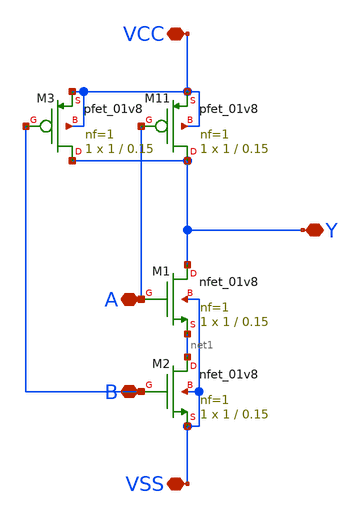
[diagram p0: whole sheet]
** sch_path: logic gates/nand.sch
**.subckt nand VCC VSS Y A B
*.iopin VCC
*.iopin VSS
*.iopin Y
*.iopin A
*.iopin B
XM2 net1 B VSS VSS sky130_fd_pr__nfet_01v8 L=0.15 W=1 nf=1 ad='int((1 + 1)/2) * 1 / 1 * 0.29' as='int((1 + 2)/2) * 1 / 1 * 0.29'
+ pd='2*int((1 + 1)/2) * (1 / 1 + 0.29)' ps='2*int((1 + 2)/2) * (1 / 1 + 0.29)' nrd='0.29 / 1 ' nrs='0.29 / 1 '
+ sa=0 sb=0 sd=0 mult=1 m=1
XM11 Y A VCC VCC sky130_fd_pr__pfet_01v8 L=0.15 W=1 nf=1 ad='int((nf+1)/2) * W/nf * 0.29' as='int((nf+2)/2) * W/nf * 0.29'
+ pd='2*int((nf+1)/2) * (W/nf + 0.29)' ps='2*int((nf+2)/2) * (W/nf + 0.29)' nrd='0.29 / W' nrs='0.29 / W'
+ sa=0 sb=0 sd=0 mult=1 m=1
XM1 Y A net1 VSS sky130_fd_pr__nfet_01v8 L=0.15 W=1 nf=1 ad='int((1 + 1)/2) * 1 / 1 * 0.29' as='int((1 + 2)/2) * 1 / 1 * 0.29'
+ pd='2*int((1 + 1)/2) * (1 / 1 + 0.29)' ps='2*int((1 + 2)/2) * (1 / 1 + 0.29)' nrd='0.29 / 1 ' nrs='0.29 / 1 '
+ sa=0 sb=0 sd=0 mult=1 m=1
XM3 Y B VCC VCC sky130_fd_pr__pfet_01v8 L=0.15 W=1 nf=1 ad='int((nf+1)/2) * W/nf * 0.29' as='int((nf+2)/2) * W/nf * 0.29'
+ pd='2*int((nf+1)/2) * (W/nf + 0.29)' ps='2*int((nf+2)/2) * (W/nf + 0.29)' nrd='0.29 / W' nrs='0.29 / W'
+ sa=0 sb=0 sd=0 mult=1 m=1
**.ends
.end
